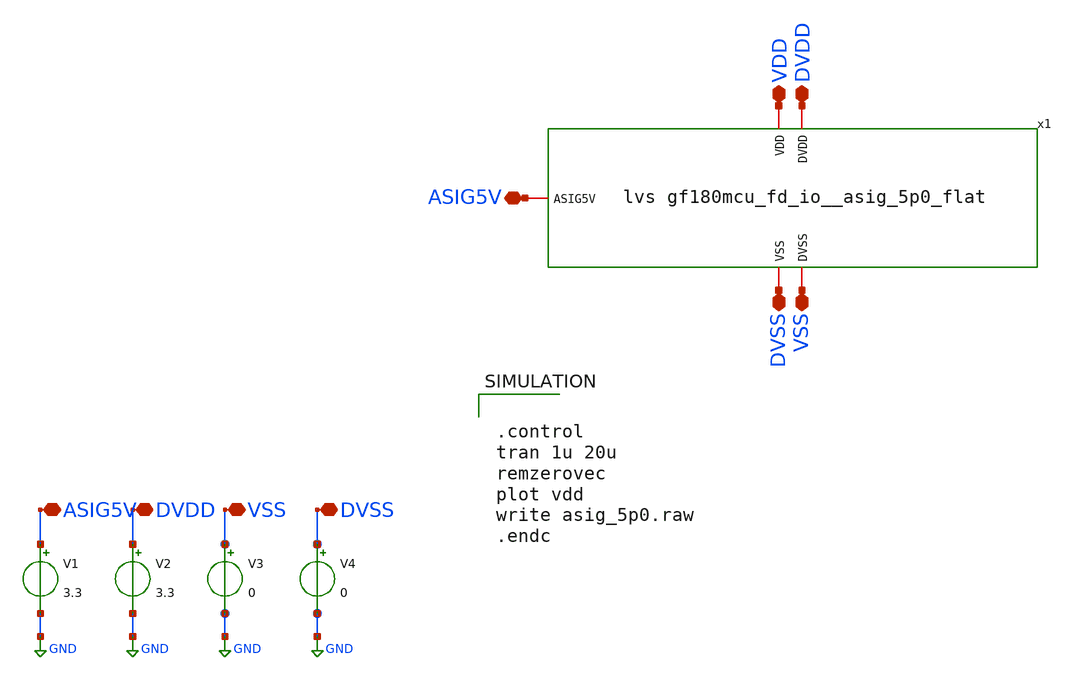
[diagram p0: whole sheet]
** sch_path: test/asig_5p0/asig_5p0.sch

.include $env(PDK_ROOT)/gf180mcuD/libs.tech/ngspice/design.ngspice
.lib $env(PDK_ROOT)/$env(PDK)/libs.tech/ngspice/sm141064.ngspice typical
.lib $env(PDK_ROOT)/$env(PDK)/libs.tech/ngspice/sm141064.ngspice diode_typical
.lib $env(PDK_ROOT)/$env(PDK)/libs.tech/ngspice/sm141064.ngspice res_typical
.lib $env(PDK_ROOT)/$env(PDK)/libs.tech/ngspice/sm141064.ngspice bjt_typical
.lib $env(PDK_ROOT)/$env(PDK)/libs.tech/ngspice/sm141064.ngspice mimcap_typical
.lib $env(PDK_ROOT)/$env(PDK)/libs.tech/ngspice/sm141064.ngspice moscap_typical


.control
tran 1u 20u
remzerovec
plot vdd
write asig_5p0.raw
.endc


**.subckt asig_5p0 ASIG5V DVDD VSS DVSS DVSS VSS DVDD ASIG5V VDD
*.iopin ASIG5V
*.iopin DVDD
*.iopin VSS
*.iopin DVSS
*.iopin DVSS
*.iopin VSS
*.iopin DVDD
*.iopin ASIG5V
*.iopin VDD
V1 ASIG5V GND 3.3
V2 DVDD GND 3.3
V3 VSS GND 0
V4 DVSS GND 0
x1 VDD DVDD ASIG5V DVSS VSS gf180mcu_fd_io__asig_5p0_flat
**.ends

* expanding   symbol:  lvs/gf180mcu_fd_io__asig_5p0_flat.sym # of pins=5
** sym_path: extraction/lvs/gf180mcu_fd_io__asig_5p0_flat.sym
.include [abs_sym_path lvs/gf180mcu_fd_io__asig_5p0.cir]
.GLOBAL GND
.end
